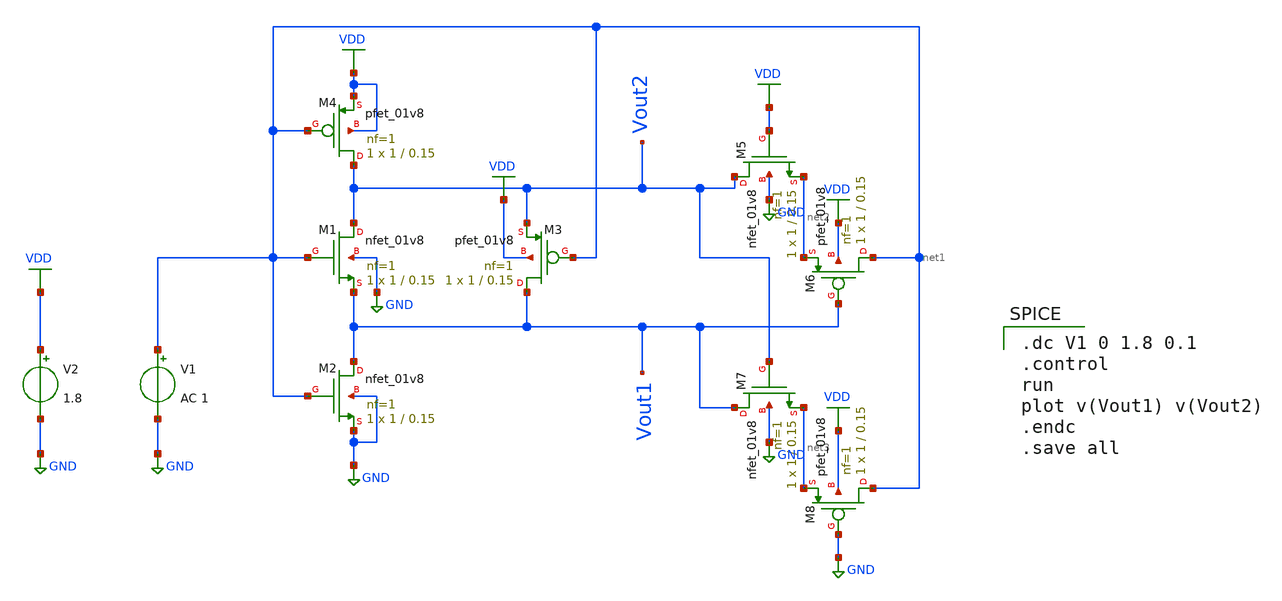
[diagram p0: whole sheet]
** sch_path: LIQAF circuit/single stage LIQAF.sch
**.subckt single stage LIQAF
XM1 Vout2 net1 Vout1 GND sky130_fd_pr__nfet_01v8 L=0.15 W=1 nf=1 ad='int((nf+1)/2) * W/nf * 0.29' as='int((nf+2)/2) * W/nf * 0.29'
+ pd='2*int((nf+1)/2) * (W/nf + 0.29)' ps='2*int((nf+2)/2) * (W/nf + 0.29)' nrd='0.29 / W' nrs='0.29 / W'
+ sa=0 sb=0 sd=0 mult=1 m=1
V1 net1 GND AC 1
V2 VDD GND 1.8
XM2 Vout1 net1 GND GND sky130_fd_pr__nfet_01v8 L=0.15 W=1 nf=1 ad='int((nf+1)/2) * W/nf * 0.29' as='int((nf+2)/2) * W/nf * 0.29'
+ pd='2*int((nf+1)/2) * (W/nf + 0.29)' ps='2*int((nf+2)/2) * (W/nf + 0.29)' nrd='0.29 / W' nrs='0.29 / W'
+ sa=0 sb=0 sd=0 mult=1 m=1
XM3 Vout1 net1 Vout2 VDD sky130_fd_pr__pfet_01v8 L=0.15 W=1 nf=1 ad='int((nf+1)/2) * W/nf * 0.29' as='int((nf+2)/2) * W/nf * 0.29'
+ pd='2*int((nf+1)/2) * (W/nf + 0.29)' ps='2*int((nf+2)/2) * (W/nf + 0.29)' nrd='0.29 / W' nrs='0.29 / W'
+ sa=0 sb=0 sd=0 mult=1 m=1
XM4 Vout2 net1 VDD VDD sky130_fd_pr__pfet_01v8 L=0.15 W=1 nf=1 ad='int((nf+1)/2) * W/nf * 0.29' as='int((nf+2)/2) * W/nf * 0.29'
+ pd='2*int((nf+1)/2) * (W/nf + 0.29)' ps='2*int((nf+2)/2) * (W/nf + 0.29)' nrd='0.29 / W' nrs='0.29 / W'
+ sa=0 sb=0 sd=0 mult=1 m=1
XM5 Vout2 VDD net2 GND sky130_fd_pr__nfet_01v8 L=0.15 W=1 nf=1 ad='int((nf+1)/2) * W/nf * 0.29' as='int((nf+2)/2) * W/nf * 0.29'
+ pd='2*int((nf+1)/2) * (W/nf + 0.29)' ps='2*int((nf+2)/2) * (W/nf + 0.29)' nrd='0.29 / W' nrs='0.29 / W'
+ sa=0 sb=0 sd=0 mult=1 m=1
XM6 net1 Vout1 net2 VDD sky130_fd_pr__pfet_01v8 L=0.15 W=1 nf=1 ad='int((nf+1)/2) * W/nf * 0.29' as='int((nf+2)/2) * W/nf * 0.29'
+ pd='2*int((nf+1)/2) * (W/nf + 0.29)' ps='2*int((nf+2)/2) * (W/nf + 0.29)' nrd='0.29 / W' nrs='0.29 / W'
+ sa=0 sb=0 sd=0 mult=1 m=1
XM7 Vout1 Vout2 net3 GND sky130_fd_pr__nfet_01v8 L=0.15 W=1 nf=1 ad='int((nf+1)/2) * W/nf * 0.29' as='int((nf+2)/2) * W/nf * 0.29'
+ pd='2*int((nf+1)/2) * (W/nf + 0.29)' ps='2*int((nf+2)/2) * (W/nf + 0.29)' nrd='0.29 / W' nrs='0.29 / W'
+ sa=0 sb=0 sd=0 mult=1 m=1
XM8 net1 GND net3 VDD sky130_fd_pr__pfet_01v8 L=0.15 W=1 nf=1 ad='int((nf+1)/2) * W/nf * 0.29' as='int((nf+2)/2) * W/nf * 0.29'
+ pd='2*int((nf+1)/2) * (W/nf + 0.29)' ps='2*int((nf+2)/2) * (W/nf + 0.29)' nrd='0.29 / W' nrs='0.29 / W'
+ sa=0 sb=0 sd=0 mult=1 m=1
**** begin user architecture code
 ** manual skywater pdks install (with patches applied)
* .lib $::SKYWATER_MODELS/models/sky130.lib.spice tt

** opencircuitdesign pdks install
.lib $::SKYWATER_MODELS/sky130.lib.spice tt

.param mc_mm_switch=0
.param mc_pr_switch=0


.dc V1 0 1.8 0.1
.control
run
plot v(Vout1) v(Vout2)
.endc
.save all

**** end user architecture code
**.ends
.GLOBAL GND
.GLOBAL VDD
.end
